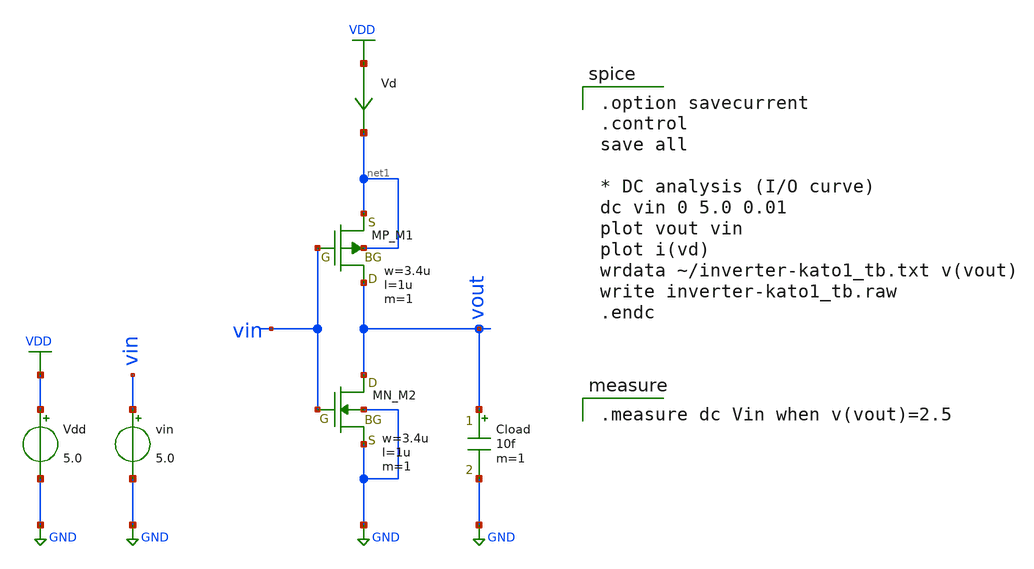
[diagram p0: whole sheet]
** sch_path: inverter/kato/inverter_kato1_tb.sch
**.subckt inverter_kato1_tb
XM1 vout vin net1 net1 PMOS w=3.4u l=1u nrd=0 nrs=0 m=1
XM2 vout vin GND GND NMOS w=3.4u l=1u nrd=0 nrs=0 m=1
Cload vout GND 10f m=1
Vdd VDD GND 5.0
vin vin GND 5.0
Vd VDD net1 0
.save i(vd)
**** begin user architecture code
 .include $::LIB/ip62_models

.option savecurrent
.control
save all

* DC analysis (I/O curve)
dc vin 0 5.0 0.01
plot vout vin
plot i(vd)
wrdata ~/inverter-kato1_tb.txt v(vout)
write inverter-kato1_tb.raw
.endc


.measure dc Vin when v(vout)=2.5

**** end user architecture code
**.ends
.GLOBAL GND
.GLOBAL VDD
.end
